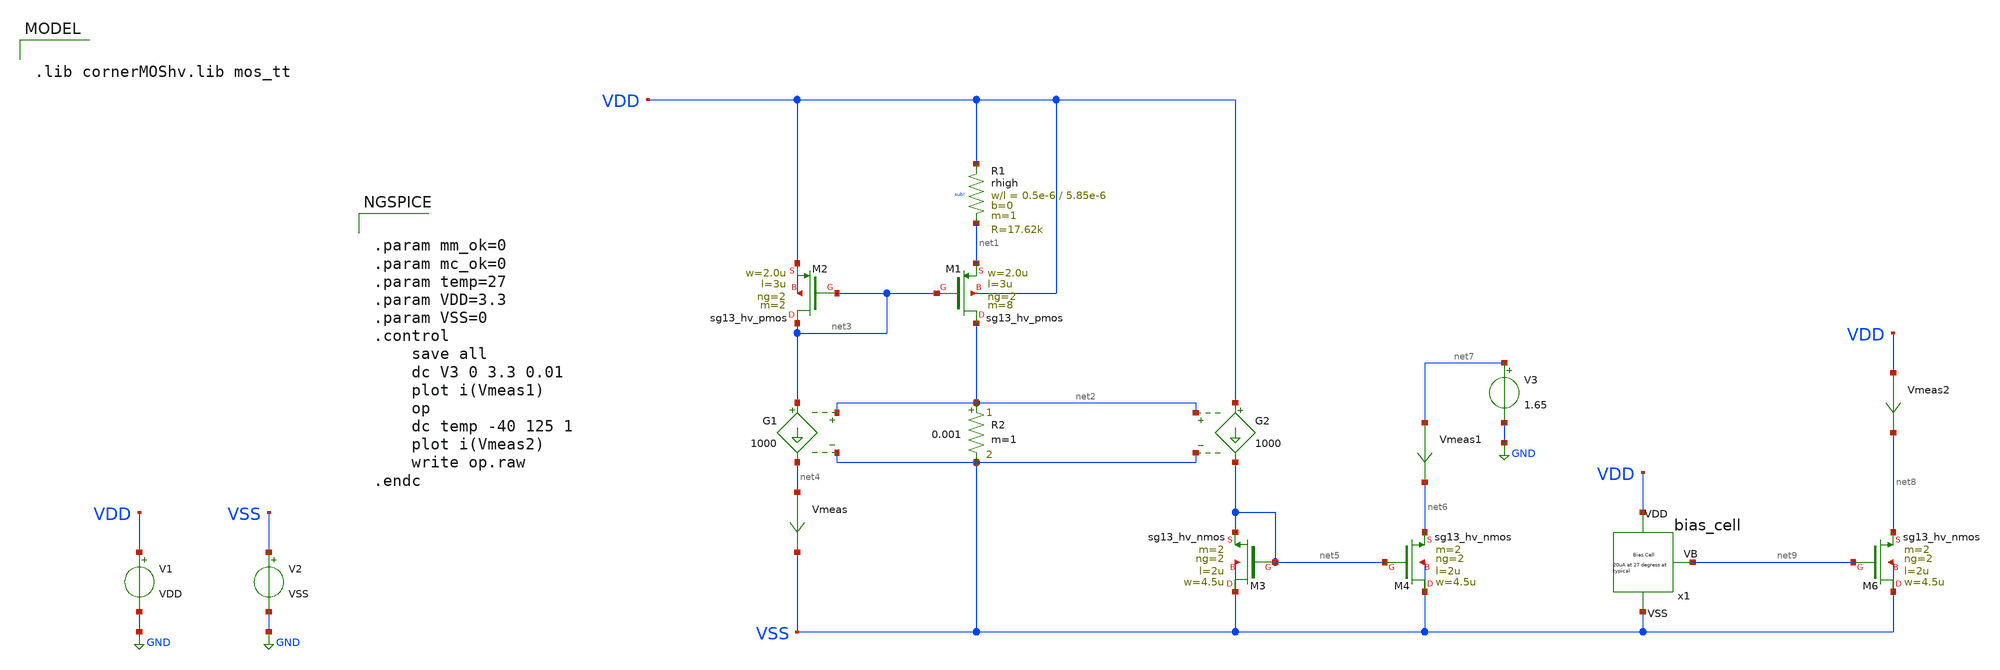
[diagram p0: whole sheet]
** sch_path: Learning/fully_differencial/Indirect_Compensation_Techniques_for_Three_Stage_Fully_Differential_Op_amps_IHP130/testbenches/transimpedance_cell_tb_.sch
**.subckt transimpedance_cell_tb_
XR1 VDD net1 sub! rhigh w=0.5e-6 l=5.85e-6 m=1 b=0 mm_ok=1
R2 net2 VSS 0.001 m=1
G1 net3 net4 net2 VSS 1000
V1 VDD GND VDD
V2 VSS GND VSS
XM1 net2 net3 net1 VDD sg13_hv_pmos w=2.0u l=3u ng=2 m=8 mm_ok=1
XM2 net3 net3 VDD VDD sg13_hv_pmos w=2.0u l=3u ng=2 m=2 mm_ok=1
Vmeas net4 VSS 0
.save i(vmeas)
G2 VDD net5 net2 VSS 1000
XM3 VSS net5 net5 VSS sg13_hv_nmos w=4.5u l=2u ng=2 m=2 mm_ok=1
Vmeas1 net7 net6 0
.save i(vmeas1)
V3 net7 GND 1.65
XM4 VSS net5 net6 VSS sg13_hv_nmos w=4.5u l=2u ng=2 m=2 mm_ok=1
XM6 VSS net9 net8 VSS sg13_hv_nmos w=4.5u l=2u ng=2 m=2 mm_ok=1
Vmeas2 VDD net8 0
.save i(vmeas2)
x1 VDD VSS net9 bias_cell
**** begin user architecture code


.param mm_ok=0
.param mc_ok=0
.param temp=27
.param VDD=3.3
.param VSS=0
.control
	save all
	dc V3 0 3.3 0.01
	plot i(Vmeas1)
	op
	dc temp -40 125 1
	plot i(Vmeas2)
	write op.raw
.endc



.lib cornerMOShv.lib mos_tt


.lib $::SG13G2_MODELS/cornerRES.lib res_typ

**** end user architecture code
**.ends

* expanding   symbol:  ihp-sg13g2/FD_opamp001/bias_cell.sym # of pins=3
** sym_path: my_ip/LIB/ihp-sg13g2/FD_opamp001/bias_cell.sym
** sch_path: my_ip/LIB/ihp-sg13g2/FD_opamp001/bias_cell.sch
.subckt bias_cell VDD VSS VB
*.iopin VDD
*.iopin VSS
*.iopin VB
XM5 VSS VB net4 VSS sg13_hv_nmos w=4.5u l=2u ng=2 m=2 mm_ok=1
XM6 VSS VB VB VSS sg13_hv_nmos w=4.5u l=2u ng=2 m=2 mm_ok=1
XR3 VDD net1 sub! rhigh w=0.5e-6 l=1.95e-6 m=1 b=0 mm_ok=1
XM7 net3 net2 net1 VDD sg13_hv_pmos w=2.0u l=3u ng=2 m=8 mm_ok=1
XM8 net2 net2 VDD VDD sg13_hv_pmos w=2.0u l=3u ng=2 m=2 mm_ok=1
XM9 net4 net4 net2 VDD sg13_hv_pmos w=2.0u l=3u ng=2 m=2 mm_ok=1
XM10 net5 net4 net3 VDD sg13_hv_pmos w=2.0u l=3u ng=2 m=2 mm_ok=1
Vmeas2 net5 VB 0
.save i(vmeas2)
.ends

.GLOBAL GND
.end
